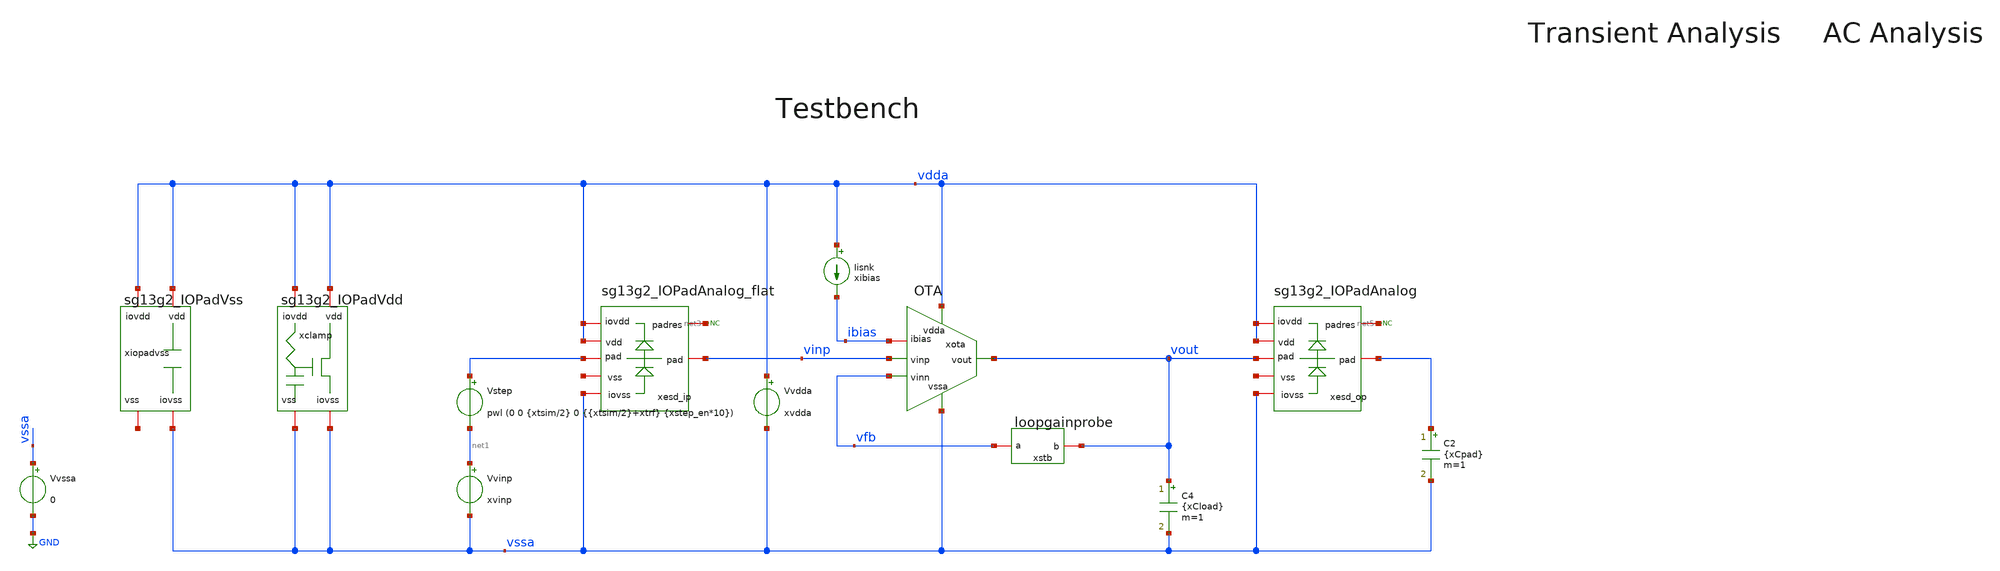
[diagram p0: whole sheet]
** sch_path: tb_OTA_1stage_ihp/tb_OTA_noPEX.sch
**.subckt tb_OTA_noPEX
Vvdda vdda vssa xvdda
Iisnk vdda ibias xibias
xota vdda vinp vfb vssa vout ibias OTA
Vstep vinp net1 pwl (0 0 {xtsim/2} 0 {{xtsim/2}+xtrf} {xstep_en*10})
Vvinp net1 vssa xvinp
Vvssa vssa GND 0
xstb vfb vout loopgainprobe
xclamp vdda vssa vdda vssa sg13g2_IOPadVdd
xiopadvss vdda vssa vdda net2 sg13g2_IOPadVss
* noconn #net3
xesd_ip vdda vssa net3 vdda vinp net4 sg13g2_IOPadAnalog_flat
xesd_op vdda vssa net5 vdda vout net6 sg13g2_IOPadAnalog
C2 vout vssa {xCpad} m=1
* noconn #net5
C4 vout vssa {xCload} m=1
**** begin user architecture code

** opencircuitdesign pdks install
.lib /home/slice/pdk/iHP/IHP-Open-PDK/ihp-sg13g2/libs.tech/ngspice/models/cornerMOSlv.lib mos_tt
*.lib /home/slice/pdk/iHP/IHP-Open-PDK/ihp-sg13g2/libs.tech/ngspice/models/sg13g2_moshv_mod.lib
.lib /home/slice/pdk/iHP/IHP-Open-PDK/ihp-sg13g2/libs.tech/ngspice/models/cornerMOShv.lib mos_tt
.lib /home/slice/pdk/iHP/IHP-Open-PDK/ihp-sg13g2/libs.tech/ngspice/models/cornerRES.lib res_typ
.include /home/slice/pdk/iHP/IHP-Open-PDK/ihp-sg13g2/libs.tech/ngspice/models/diodes.lib
*.lib /home/slice/xschem/tb_OTA_1stage_ihp/cornerRES.lib res_typ
*.lib /home/slice/xschem/tb_OTA_1stage_ihp/resistors_mod.lib

*.model
*+ /home/slice/pdk/iHP/IHP-Open-PDK/ihp-sg13g2/libs.tech/ngspice/models/sg13g2_moshv_mod.lib/sg13_hv_pmos

*.model /home/slice/Desktop/acm2/MOSFET_model/Verilog-A/NMOS_ACM_2V0.va
*.model /home/slice/Desktop/acm2/MOSFET_model/Verilog-A/PMOS_ACM_2V0.va

* Parameters
.param xvdda = 1.8
.param xvinp = 1
.param xibias = 40u
.param xCload = 0.75p
.param xCpad = 100f
.param xgm_dp = 1e-3
.param xRin = 1/xgm_dp
.param xCout = 1p
.param xRout = 1e6
.param xtrf = 50p
.param xtsim = 5u
.csparam xtsim_var = 'xtsim'
.param xstep_en = 1

* vlogA instantiation
.model OTA_vcvs OTA_vcvs


  ** must save the below for DCOP analysis to be back annotated onto the schematic
  .option savecurrents

  .include tb_OTA.save
  *.save all
  .save v(vout) v(vinp) v(vfb) v(vdda) v(xota.pdio) v(xota.vtail) v(vout_pad)
  .save i(v.xota.Virhs) i(v.xota.Vitail) i(xota.vdda) i(v.Vdda) i(xesd_ip.pad) i(v.Vstep)
  .save i(@n.xota.xm6.nsg13_lv_pmos[ids])


  .control
  let xtsim = $&xtsim_var
  pre_osdi OTA_vcvs.osdi
  save all

** 1. DCOP ANALYSIS **

  op
 * set filetype=ascii
  remzerovec
  write tb_OTA_op.raw

** 2. TRAN ANALYSIS **

  tran 1n $&xtsim
  echo --
  echo TSIM VALUE
    echo $&xtsim
    echo --
  *set filetype=ascii
  remzerovec
  write tb_OTA_tran.raw

** 3. AC ANALYSIS **

  alter i.xstb.Ii acmag=0
  alter v.xstb.Vi acmag=1

  ac dec 10 1 100G

  remzerovec
  write tb_OTA_1stage_ac1.raw

  alter i.xstb.Ii acmag=1
  alter v.xstb.Vi acmag=0

  ac dec 10 1 100G

  * use this line if you want the phase response to start at 180deg
  *let av = {1/(1-1/(2*(ac1.i(v.xstb.Vi)*ac2.v(xstb.x)-ac1.v(xstb.x)*ac2.i(v.xstb.Vi))+ac1.v(xstb.x)+ac2.i(v.xstb.Vi)))}

  * use this line if you want the phase response to start at 0deg (more conventional and directly
+ corresponds to Franks derivation)
  let av = {1/(1/(2*(ac1.i(v.xstb.Vi)*ac2.v(xstb.x)-ac1.v(xstb.x)*ac2.i(v.xstb.Vi))+ac1.v(xstb.x)+ac2.i(v.xstb.Vi))-1)}

  remzerovec
  write tb_OTA_1stage_ac2.raw

  ** 4. MEASURES **

  let n45_rads = -45*(pi/180)
  meas AC Av_0 FIND vdb(av) AT=10
  echo --
  meas AC BW WHEN vp(av)=n45_rads CROSS=1
  echo --
  meas AC Av_BW FIND vdb(av) WHEN vp(av)=n45_rads CROSS=1
  echo --
  meas AC ULGF WHEN vdb(av)=0
  echo --
  meas AC ULGF_phi_rads FIND vp(av) WHEN vdb(av)=0 CROSS=1
  let ULGF_phi_deg = ULGF_phi_rads*(180/pi)
  print ULGF_phi_deg
  let PM = 180+ULGF_phi_deg
  print PM
  echo --
  * putting in -170 since this is a 2nd-order system so doesnt ever achieve -180
  let n180_rads = -170*(pi/180)
  meas AC GM FIND vdb(av) WHEN vp(av)=n180_rads CROSS=1

  setplot
*quit 0
.endc




**** end user architecture code
**.ends
.GLOBAL GND
.end
